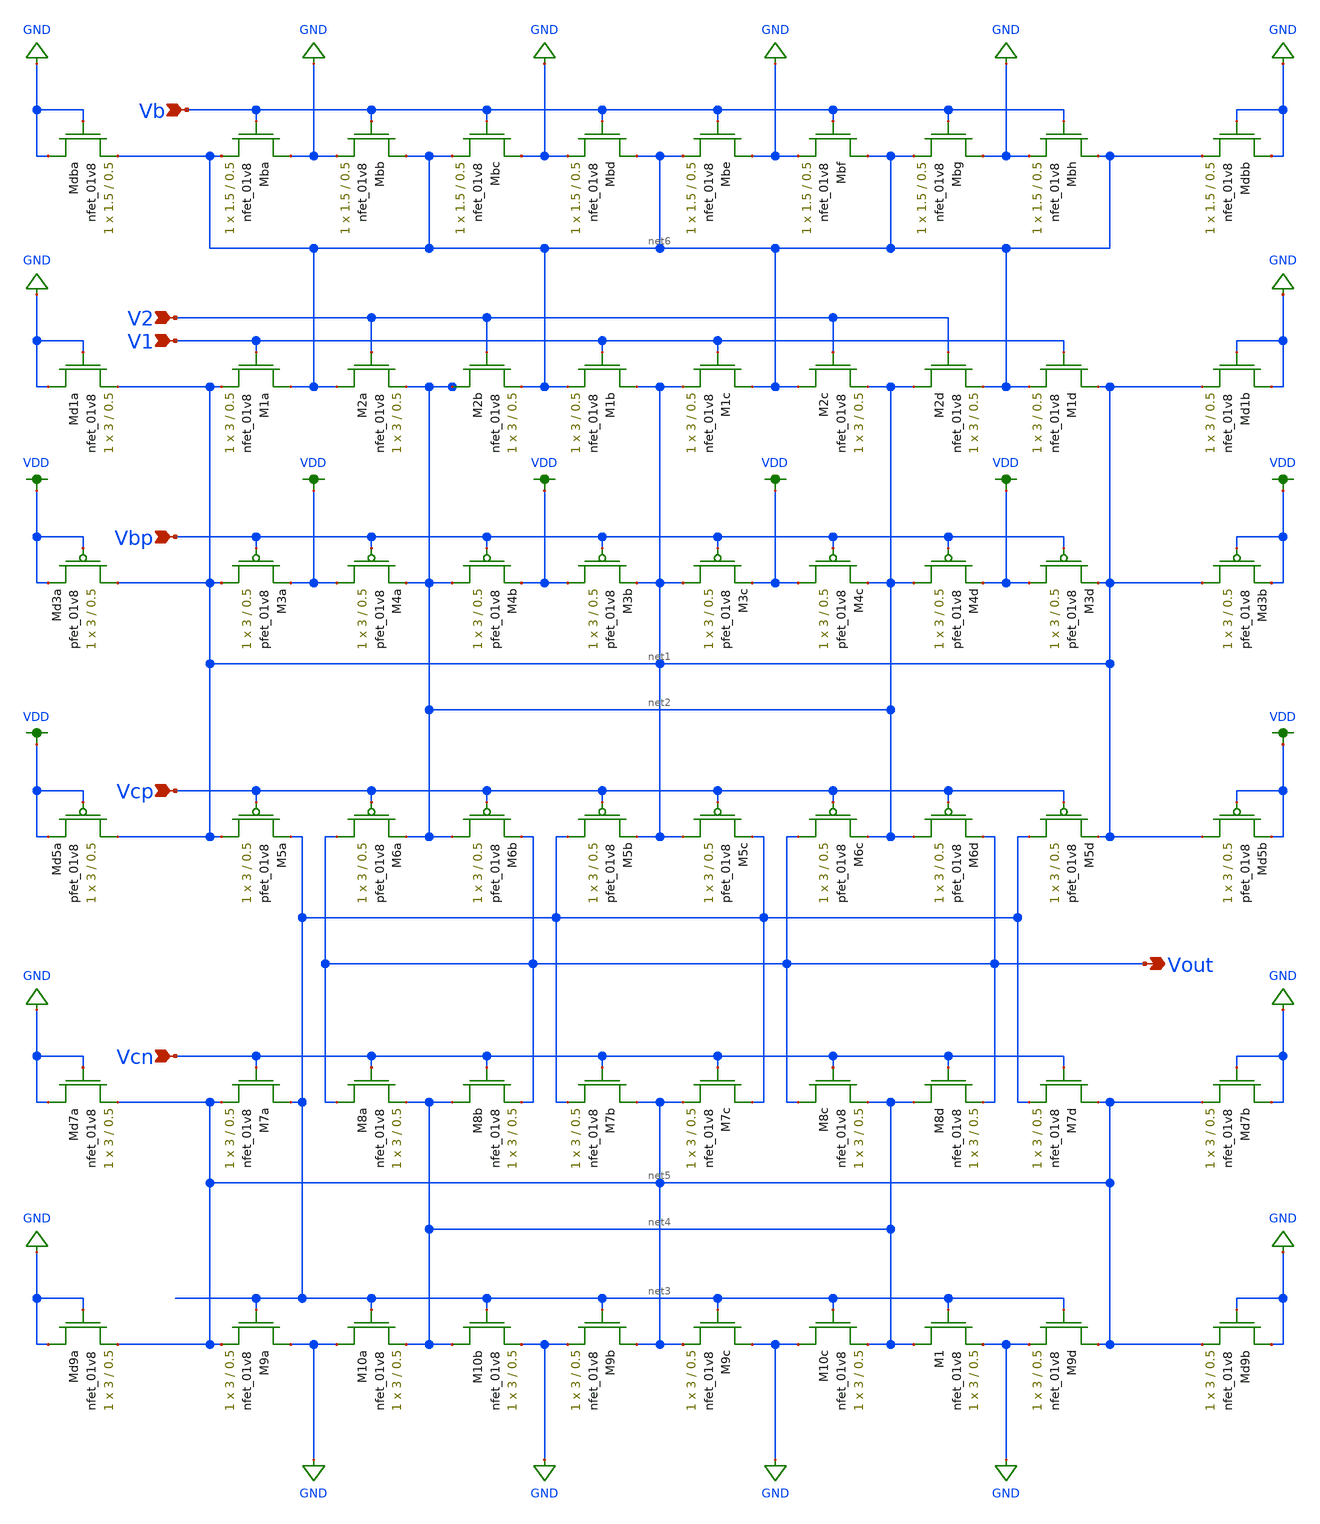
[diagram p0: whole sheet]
** sch_path: mp3/xschem/opamp_layout.sch
**.subckt opamp_layout Vbp Vcp Vcn V2 V1 Vb Vout
*.ipin Vbp
*.ipin Vcp
*.ipin Vcn
*.ipin V2
*.ipin V1
*.ipin Vb
*.opin Vout
XM1a net6 V1 net1 GND sky130_fd_pr__nfet_01v8 L=0.5 W=3 nf=1 ad='int((nf+1)/2) * W/nf * 0.29' as='int((nf+2)/2) * W/nf * 0.29'
+ pd='2*int((nf+1)/2) * (W/nf + 0.29)' ps='2*int((nf+2)/2) * (W/nf + 0.29)' nrd='0.29 / W' nrs='0.29 / W'
+ sa=0 sb=0 sd=0 mult=1 m=1
XM1b net1 V1 net6 GND sky130_fd_pr__nfet_01v8 L=0.5 W=3 nf=1 ad='int((nf+1)/2) * W/nf * 0.29' as='int((nf+2)/2) * W/nf * 0.29'
+ pd='2*int((nf+1)/2) * (W/nf + 0.29)' ps='2*int((nf+2)/2) * (W/nf + 0.29)' nrd='0.29 / W' nrs='0.29 / W'
+ sa=0 sb=0 sd=0 mult=1 m=1
XM1c net6 V1 net1 GND sky130_fd_pr__nfet_01v8 L=0.5 W=3 nf=1 ad='int((nf+1)/2) * W/nf * 0.29' as='int((nf+2)/2) * W/nf * 0.29'
+ pd='2*int((nf+1)/2) * (W/nf + 0.29)' ps='2*int((nf+2)/2) * (W/nf + 0.29)' nrd='0.29 / W' nrs='0.29 / W'
+ sa=0 sb=0 sd=0 mult=1 m=1
XM1d net1 V1 net6 GND sky130_fd_pr__nfet_01v8 L=0.5 W=3 nf=1 ad='int((nf+1)/2) * W/nf * 0.29' as='int((nf+2)/2) * W/nf * 0.29'
+ pd='2*int((nf+1)/2) * (W/nf + 0.29)' ps='2*int((nf+2)/2) * (W/nf + 0.29)' nrd='0.29 / W' nrs='0.29 / W'
+ sa=0 sb=0 sd=0 mult=1 m=1
XM2a net6 V2 net2 GND sky130_fd_pr__nfet_01v8 L=0.5 W=3 nf=1 ad='int((nf+1)/2) * W/nf * 0.29' as='int((nf+2)/2) * W/nf * 0.29'
+ pd='2*int((nf+1)/2) * (W/nf + 0.29)' ps='2*int((nf+2)/2) * (W/nf + 0.29)' nrd='0.29 / W' nrs='0.29 / W'
+ sa=0 sb=0 sd=0 mult=1 m=1
XM2b net2 V2 net6 GND sky130_fd_pr__nfet_01v8 L=0.5 W=3 nf=1 ad='int((nf+1)/2) * W/nf * 0.29' as='int((nf+2)/2) * W/nf * 0.29'
+ pd='2*int((nf+1)/2) * (W/nf + 0.29)' ps='2*int((nf+2)/2) * (W/nf + 0.29)' nrd='0.29 / W' nrs='0.29 / W'
+ sa=0 sb=0 sd=0 mult=1 m=1
XM2c net6 V2 net2 GND sky130_fd_pr__nfet_01v8 L=0.5 W=3 nf=1 ad='int((nf+1)/2) * W/nf * 0.29' as='int((nf+2)/2) * W/nf * 0.29'
+ pd='2*int((nf+1)/2) * (W/nf + 0.29)' ps='2*int((nf+2)/2) * (W/nf + 0.29)' nrd='0.29 / W' nrs='0.29 / W'
+ sa=0 sb=0 sd=0 mult=1 m=1
XM2d net2 V2 net6 GND sky130_fd_pr__nfet_01v8 L=0.5 W=3 nf=1 ad='int((nf+1)/2) * W/nf * 0.29' as='int((nf+2)/2) * W/nf * 0.29'
+ pd='2*int((nf+1)/2) * (W/nf + 0.29)' ps='2*int((nf+2)/2) * (W/nf + 0.29)' nrd='0.29 / W' nrs='0.29 / W'
+ sa=0 sb=0 sd=0 mult=1 m=1
XMba GND Vb net6 GND sky130_fd_pr__nfet_01v8 L=0.5 W=1.5 nf=1 ad='int((nf+1)/2) * W/nf * 0.29' as='int((nf+2)/2) * W/nf * 0.29'
+ pd='2*int((nf+1)/2) * (W/nf + 0.29)' ps='2*int((nf+2)/2) * (W/nf + 0.29)' nrd='0.29 / W' nrs='0.29 / W'
+ sa=0 sb=0 sd=0 mult=1 m=1
XMbb net6 Vb GND GND sky130_fd_pr__nfet_01v8 L=0.5 W=1.5 nf=1 ad='int((nf+1)/2) * W/nf * 0.29' as='int((nf+2)/2) * W/nf * 0.29'
+ pd='2*int((nf+1)/2) * (W/nf + 0.29)' ps='2*int((nf+2)/2) * (W/nf + 0.29)' nrd='0.29 / W' nrs='0.29 / W'
+ sa=0 sb=0 sd=0 mult=1 m=1
XMbc GND Vb net6 GND sky130_fd_pr__nfet_01v8 L=0.5 W=1.5 nf=1 ad='int((nf+1)/2) * W/nf * 0.29' as='int((nf+2)/2) * W/nf * 0.29'
+ pd='2*int((nf+1)/2) * (W/nf + 0.29)' ps='2*int((nf+2)/2) * (W/nf + 0.29)' nrd='0.29 / W' nrs='0.29 / W'
+ sa=0 sb=0 sd=0 mult=1 m=1
XMbd net6 Vb GND GND sky130_fd_pr__nfet_01v8 L=0.5 W=1.5 nf=1 ad='int((nf+1)/2) * W/nf * 0.29' as='int((nf+2)/2) * W/nf * 0.29'
+ pd='2*int((nf+1)/2) * (W/nf + 0.29)' ps='2*int((nf+2)/2) * (W/nf + 0.29)' nrd='0.29 / W' nrs='0.29 / W'
+ sa=0 sb=0 sd=0 mult=1 m=1
XMbe GND Vb net6 GND sky130_fd_pr__nfet_01v8 L=0.5 W=1.5 nf=1 ad='int((nf+1)/2) * W/nf * 0.29' as='int((nf+2)/2) * W/nf * 0.29'
+ pd='2*int((nf+1)/2) * (W/nf + 0.29)' ps='2*int((nf+2)/2) * (W/nf + 0.29)' nrd='0.29 / W' nrs='0.29 / W'
+ sa=0 sb=0 sd=0 mult=1 m=1
XMbf net6 Vb GND GND sky130_fd_pr__nfet_01v8 L=0.5 W=1.5 nf=1 ad='int((nf+1)/2) * W/nf * 0.29' as='int((nf+2)/2) * W/nf * 0.29'
+ pd='2*int((nf+1)/2) * (W/nf + 0.29)' ps='2*int((nf+2)/2) * (W/nf + 0.29)' nrd='0.29 / W' nrs='0.29 / W'
+ sa=0 sb=0 sd=0 mult=1 m=1
XMbg GND Vb net6 GND sky130_fd_pr__nfet_01v8 L=0.5 W=1.5 nf=1 ad='int((nf+1)/2) * W/nf * 0.29' as='int((nf+2)/2) * W/nf * 0.29'
+ pd='2*int((nf+1)/2) * (W/nf + 0.29)' ps='2*int((nf+2)/2) * (W/nf + 0.29)' nrd='0.29 / W' nrs='0.29 / W'
+ sa=0 sb=0 sd=0 mult=1 m=1
XMbh net6 Vb GND GND sky130_fd_pr__nfet_01v8 L=0.5 W=1.5 nf=1 ad='int((nf+1)/2) * W/nf * 0.29' as='int((nf+2)/2) * W/nf * 0.29'
+ pd='2*int((nf+1)/2) * (W/nf + 0.29)' ps='2*int((nf+2)/2) * (W/nf + 0.29)' nrd='0.29 / W' nrs='0.29 / W'
+ sa=0 sb=0 sd=0 mult=1 m=1
XM7a net3 Vcn net5 GND sky130_fd_pr__nfet_01v8 L=0.5 W=3 nf=1 ad='int((nf+1)/2) * W/nf * 0.29' as='int((nf+2)/2) * W/nf * 0.29'
+ pd='2*int((nf+1)/2) * (W/nf + 0.29)' ps='2*int((nf+2)/2) * (W/nf + 0.29)' nrd='0.29 / W' nrs='0.29 / W'
+ sa=0 sb=0 sd=0 mult=1 m=1
XM7b net5 Vcn net3 GND sky130_fd_pr__nfet_01v8 L=0.5 W=3 nf=1 ad='int((nf+1)/2) * W/nf * 0.29' as='int((nf+2)/2) * W/nf * 0.29'
+ pd='2*int((nf+1)/2) * (W/nf + 0.29)' ps='2*int((nf+2)/2) * (W/nf + 0.29)' nrd='0.29 / W' nrs='0.29 / W'
+ sa=0 sb=0 sd=0 mult=1 m=1
XM7c net3 Vcn net5 GND sky130_fd_pr__nfet_01v8 L=0.5 W=3 nf=1 ad='int((nf+1)/2) * W/nf * 0.29' as='int((nf+2)/2) * W/nf * 0.29'
+ pd='2*int((nf+1)/2) * (W/nf + 0.29)' ps='2*int((nf+2)/2) * (W/nf + 0.29)' nrd='0.29 / W' nrs='0.29 / W'
+ sa=0 sb=0 sd=0 mult=1 m=1
XM7d net5 Vcn net3 GND sky130_fd_pr__nfet_01v8 L=0.5 W=3 nf=1 ad='int((nf+1)/2) * W/nf * 0.29' as='int((nf+2)/2) * W/nf * 0.29'
+ pd='2*int((nf+1)/2) * (W/nf + 0.29)' ps='2*int((nf+2)/2) * (W/nf + 0.29)' nrd='0.29 / W' nrs='0.29 / W'
+ sa=0 sb=0 sd=0 mult=1 m=1
XM8a Vout Vcn net4 GND sky130_fd_pr__nfet_01v8 L=0.5 W=3 nf=1 ad='int((nf+1)/2) * W/nf * 0.29' as='int((nf+2)/2) * W/nf * 0.29'
+ pd='2*int((nf+1)/2) * (W/nf + 0.29)' ps='2*int((nf+2)/2) * (W/nf + 0.29)' nrd='0.29 / W' nrs='0.29 / W'
+ sa=0 sb=0 sd=0 mult=1 m=1
XM8b net4 Vcn Vout GND sky130_fd_pr__nfet_01v8 L=0.5 W=3 nf=1 ad='int((nf+1)/2) * W/nf * 0.29' as='int((nf+2)/2) * W/nf * 0.29'
+ pd='2*int((nf+1)/2) * (W/nf + 0.29)' ps='2*int((nf+2)/2) * (W/nf + 0.29)' nrd='0.29 / W' nrs='0.29 / W'
+ sa=0 sb=0 sd=0 mult=1 m=1
XM8c Vout Vcn net4 GND sky130_fd_pr__nfet_01v8 L=0.5 W=3 nf=1 ad='int((nf+1)/2) * W/nf * 0.29' as='int((nf+2)/2) * W/nf * 0.29'
+ pd='2*int((nf+1)/2) * (W/nf + 0.29)' ps='2*int((nf+2)/2) * (W/nf + 0.29)' nrd='0.29 / W' nrs='0.29 / W'
+ sa=0 sb=0 sd=0 mult=1 m=1
XM8d net4 Vcn Vout GND sky130_fd_pr__nfet_01v8 L=0.5 W=3 nf=1 ad='int((nf+1)/2) * W/nf * 0.29' as='int((nf+2)/2) * W/nf * 0.29'
+ pd='2*int((nf+1)/2) * (W/nf + 0.29)' ps='2*int((nf+2)/2) * (W/nf + 0.29)' nrd='0.29 / W' nrs='0.29 / W'
+ sa=0 sb=0 sd=0 mult=1 m=1
XM9a GND net3 net5 GND sky130_fd_pr__nfet_01v8 L=0.5 W=3 nf=1 ad='int((nf+1)/2) * W/nf * 0.29' as='int((nf+2)/2) * W/nf * 0.29'
+ pd='2*int((nf+1)/2) * (W/nf + 0.29)' ps='2*int((nf+2)/2) * (W/nf + 0.29)' nrd='0.29 / W' nrs='0.29 / W'
+ sa=0 sb=0 sd=0 mult=1 m=1
XM9b net5 net3 GND GND sky130_fd_pr__nfet_01v8 L=0.5 W=3 nf=1 ad='int((nf+1)/2) * W/nf * 0.29' as='int((nf+2)/2) * W/nf * 0.29'
+ pd='2*int((nf+1)/2) * (W/nf + 0.29)' ps='2*int((nf+2)/2) * (W/nf + 0.29)' nrd='0.29 / W' nrs='0.29 / W'
+ sa=0 sb=0 sd=0 mult=1 m=1
XM9c GND net3 net5 GND sky130_fd_pr__nfet_01v8 L=0.5 W=3 nf=1 ad='int((nf+1)/2) * W/nf * 0.29' as='int((nf+2)/2) * W/nf * 0.29'
+ pd='2*int((nf+1)/2) * (W/nf + 0.29)' ps='2*int((nf+2)/2) * (W/nf + 0.29)' nrd='0.29 / W' nrs='0.29 / W'
+ sa=0 sb=0 sd=0 mult=1 m=1
XM9d net5 net3 GND GND sky130_fd_pr__nfet_01v8 L=0.5 W=3 nf=1 ad='int((nf+1)/2) * W/nf * 0.29' as='int((nf+2)/2) * W/nf * 0.29'
+ pd='2*int((nf+1)/2) * (W/nf + 0.29)' ps='2*int((nf+2)/2) * (W/nf + 0.29)' nrd='0.29 / W' nrs='0.29 / W'
+ sa=0 sb=0 sd=0 mult=1 m=1
XM10a GND net3 net4 GND sky130_fd_pr__nfet_01v8 L=0.5 W=3 nf=1 ad='int((nf+1)/2) * W/nf * 0.29' as='int((nf+2)/2) * W/nf * 0.29'
+ pd='2*int((nf+1)/2) * (W/nf + 0.29)' ps='2*int((nf+2)/2) * (W/nf + 0.29)' nrd='0.29 / W' nrs='0.29 / W'
+ sa=0 sb=0 sd=0 mult=1 m=1
XM10b net4 net3 GND GND sky130_fd_pr__nfet_01v8 L=0.5 W=3 nf=1 ad='int((nf+1)/2) * W/nf * 0.29' as='int((nf+2)/2) * W/nf * 0.29'
+ pd='2*int((nf+1)/2) * (W/nf + 0.29)' ps='2*int((nf+2)/2) * (W/nf + 0.29)' nrd='0.29 / W' nrs='0.29 / W'
+ sa=0 sb=0 sd=0 mult=1 m=1
XM10c GND net3 net4 GND sky130_fd_pr__nfet_01v8 L=0.5 W=3 nf=1 ad='int((nf+1)/2) * W/nf * 0.29' as='int((nf+2)/2) * W/nf * 0.29'
+ pd='2*int((nf+1)/2) * (W/nf + 0.29)' ps='2*int((nf+2)/2) * (W/nf + 0.29)' nrd='0.29 / W' nrs='0.29 / W'
+ sa=0 sb=0 sd=0 mult=1 m=1
XM1 net4 net3 GND GND sky130_fd_pr__nfet_01v8 L=0.5 W=3 nf=1 ad='int((nf+1)/2) * W/nf * 0.29' as='int((nf+2)/2) * W/nf * 0.29'
+ pd='2*int((nf+1)/2) * (W/nf + 0.29)' ps='2*int((nf+2)/2) * (W/nf + 0.29)' nrd='0.29 / W' nrs='0.29 / W'
+ sa=0 sb=0 sd=0 mult=1 m=1
XM5a net1 Vcp net3 VDD sky130_fd_pr__pfet_01v8 L=0.5 W=3 nf=1 ad='int((nf+1)/2) * W/nf * 0.29' as='int((nf+2)/2) * W/nf * 0.29'
+ pd='2*int((nf+1)/2) * (W/nf + 0.29)' ps='2*int((nf+2)/2) * (W/nf + 0.29)' nrd='0.29 / W' nrs='0.29 / W'
+ sa=0 sb=0 sd=0 mult=1 m=1
XM5b net3 Vcp net1 VDD sky130_fd_pr__pfet_01v8 L=0.5 W=3 nf=1 ad='int((nf+1)/2) * W/nf * 0.29' as='int((nf+2)/2) * W/nf * 0.29'
+ pd='2*int((nf+1)/2) * (W/nf + 0.29)' ps='2*int((nf+2)/2) * (W/nf + 0.29)' nrd='0.29 / W' nrs='0.29 / W'
+ sa=0 sb=0 sd=0 mult=1 m=1
XM5c net1 Vcp net3 VDD sky130_fd_pr__pfet_01v8 L=0.5 W=3 nf=1 ad='int((nf+1)/2) * W/nf * 0.29' as='int((nf+2)/2) * W/nf * 0.29'
+ pd='2*int((nf+1)/2) * (W/nf + 0.29)' ps='2*int((nf+2)/2) * (W/nf + 0.29)' nrd='0.29 / W' nrs='0.29 / W'
+ sa=0 sb=0 sd=0 mult=1 m=1
XM5d net3 Vcp net1 VDD sky130_fd_pr__pfet_01v8 L=0.5 W=3 nf=1 ad='int((nf+1)/2) * W/nf * 0.29' as='int((nf+2)/2) * W/nf * 0.29'
+ pd='2*int((nf+1)/2) * (W/nf + 0.29)' ps='2*int((nf+2)/2) * (W/nf + 0.29)' nrd='0.29 / W' nrs='0.29 / W'
+ sa=0 sb=0 sd=0 mult=1 m=1
XM6a Vout Vcp net2 VDD sky130_fd_pr__pfet_01v8 L=0.5 W=3 nf=1 ad='int((nf+1)/2) * W/nf * 0.29' as='int((nf+2)/2) * W/nf * 0.29'
+ pd='2*int((nf+1)/2) * (W/nf + 0.29)' ps='2*int((nf+2)/2) * (W/nf + 0.29)' nrd='0.29 / W' nrs='0.29 / W'
+ sa=0 sb=0 sd=0 mult=1 m=1
XM6b net2 Vcp Vout VDD sky130_fd_pr__pfet_01v8 L=0.5 W=3 nf=1 ad='int((nf+1)/2) * W/nf * 0.29' as='int((nf+2)/2) * W/nf * 0.29'
+ pd='2*int((nf+1)/2) * (W/nf + 0.29)' ps='2*int((nf+2)/2) * (W/nf + 0.29)' nrd='0.29 / W' nrs='0.29 / W'
+ sa=0 sb=0 sd=0 mult=1 m=1
XM6c Vout Vcp net2 VDD sky130_fd_pr__pfet_01v8 L=0.5 W=3 nf=1 ad='int((nf+1)/2) * W/nf * 0.29' as='int((nf+2)/2) * W/nf * 0.29'
+ pd='2*int((nf+1)/2) * (W/nf + 0.29)' ps='2*int((nf+2)/2) * (W/nf + 0.29)' nrd='0.29 / W' nrs='0.29 / W'
+ sa=0 sb=0 sd=0 mult=1 m=1
XM6d net2 Vcp Vout VDD sky130_fd_pr__pfet_01v8 L=0.5 W=3 nf=1 ad='int((nf+1)/2) * W/nf * 0.29' as='int((nf+2)/2) * W/nf * 0.29'
+ pd='2*int((nf+1)/2) * (W/nf + 0.29)' ps='2*int((nf+2)/2) * (W/nf + 0.29)' nrd='0.29 / W' nrs='0.29 / W'
+ sa=0 sb=0 sd=0 mult=1 m=1
XM3a net1 Vbp VDD VDD sky130_fd_pr__pfet_01v8 L=0.5 W=3 nf=1 ad='int((nf+1)/2) * W/nf * 0.29' as='int((nf+2)/2) * W/nf * 0.29'
+ pd='2*int((nf+1)/2) * (W/nf + 0.29)' ps='2*int((nf+2)/2) * (W/nf + 0.29)' nrd='0.29 / W' nrs='0.29 / W'
+ sa=0 sb=0 sd=0 mult=1 m=1
XM3b VDD Vbp net1 VDD sky130_fd_pr__pfet_01v8 L=0.5 W=3 nf=1 ad='int((nf+1)/2) * W/nf * 0.29' as='int((nf+2)/2) * W/nf * 0.29'
+ pd='2*int((nf+1)/2) * (W/nf + 0.29)' ps='2*int((nf+2)/2) * (W/nf + 0.29)' nrd='0.29 / W' nrs='0.29 / W'
+ sa=0 sb=0 sd=0 mult=1 m=1
XM3c net1 Vbp VDD VDD sky130_fd_pr__pfet_01v8 L=0.5 W=3 nf=1 ad='int((nf+1)/2) * W/nf * 0.29' as='int((nf+2)/2) * W/nf * 0.29'
+ pd='2*int((nf+1)/2) * (W/nf + 0.29)' ps='2*int((nf+2)/2) * (W/nf + 0.29)' nrd='0.29 / W' nrs='0.29 / W'
+ sa=0 sb=0 sd=0 mult=1 m=1
XM3d VDD Vbp net1 VDD sky130_fd_pr__pfet_01v8 L=0.5 W=3 nf=1 ad='int((nf+1)/2) * W/nf * 0.29' as='int((nf+2)/2) * W/nf * 0.29'
+ pd='2*int((nf+1)/2) * (W/nf + 0.29)' ps='2*int((nf+2)/2) * (W/nf + 0.29)' nrd='0.29 / W' nrs='0.29 / W'
+ sa=0 sb=0 sd=0 mult=1 m=1
XM4a VDD Vbp net2 VDD sky130_fd_pr__pfet_01v8 L=0.5 W=3 nf=1 ad='int((nf+1)/2) * W/nf * 0.29' as='int((nf+2)/2) * W/nf * 0.29'
+ pd='2*int((nf+1)/2) * (W/nf + 0.29)' ps='2*int((nf+2)/2) * (W/nf + 0.29)' nrd='0.29 / W' nrs='0.29 / W'
+ sa=0 sb=0 sd=0 mult=1 m=1
XM4b net2 Vbp VDD VDD sky130_fd_pr__pfet_01v8 L=0.5 W=3 nf=1 ad='int((nf+1)/2) * W/nf * 0.29' as='int((nf+2)/2) * W/nf * 0.29'
+ pd='2*int((nf+1)/2) * (W/nf + 0.29)' ps='2*int((nf+2)/2) * (W/nf + 0.29)' nrd='0.29 / W' nrs='0.29 / W'
+ sa=0 sb=0 sd=0 mult=1 m=1
XM4c VDD Vbp net2 VDD sky130_fd_pr__pfet_01v8 L=0.5 W=3 nf=1 ad='int((nf+1)/2) * W/nf * 0.29' as='int((nf+2)/2) * W/nf * 0.29'
+ pd='2*int((nf+1)/2) * (W/nf + 0.29)' ps='2*int((nf+2)/2) * (W/nf + 0.29)' nrd='0.29 / W' nrs='0.29 / W'
+ sa=0 sb=0 sd=0 mult=1 m=1
XM4d net2 Vbp VDD VDD sky130_fd_pr__pfet_01v8 L=0.5 W=3 nf=1 ad='int((nf+1)/2) * W/nf * 0.29' as='int((nf+2)/2) * W/nf * 0.29'
+ pd='2*int((nf+1)/2) * (W/nf + 0.29)' ps='2*int((nf+2)/2) * (W/nf + 0.29)' nrd='0.29 / W' nrs='0.29 / W'
+ sa=0 sb=0 sd=0 mult=1 m=1
XMdbb GND GND net6 GND sky130_fd_pr__nfet_01v8 L=0.5 W=1.5 nf=1 ad='int((nf+1)/2) * W/nf * 0.29' as='int((nf+2)/2) * W/nf * 0.29'
+ pd='2*int((nf+1)/2) * (W/nf + 0.29)' ps='2*int((nf+2)/2) * (W/nf + 0.29)' nrd='0.29 / W' nrs='0.29 / W'
+ sa=0 sb=0 sd=0 mult=1 m=1
XMd1b GND GND net1 GND sky130_fd_pr__nfet_01v8 L=0.5 W=3 nf=1 ad='int((nf+1)/2) * W/nf * 0.29' as='int((nf+2)/2) * W/nf * 0.29'
+ pd='2*int((nf+1)/2) * (W/nf + 0.29)' ps='2*int((nf+2)/2) * (W/nf + 0.29)' nrd='0.29 / W' nrs='0.29 / W'
+ sa=0 sb=0 sd=0 mult=1 m=1
XMd7b GND GND net5 GND sky130_fd_pr__nfet_01v8 L=0.5 W=3 nf=1 ad='int((nf+1)/2) * W/nf * 0.29' as='int((nf+2)/2) * W/nf * 0.29'
+ pd='2*int((nf+1)/2) * (W/nf + 0.29)' ps='2*int((nf+2)/2) * (W/nf + 0.29)' nrd='0.29 / W' nrs='0.29 / W'
+ sa=0 sb=0 sd=0 mult=1 m=1
XMd9b GND GND net5 GND sky130_fd_pr__nfet_01v8 L=0.5 W=3 nf=1 ad='int((nf+1)/2) * W/nf * 0.29' as='int((nf+2)/2) * W/nf * 0.29'
+ pd='2*int((nf+1)/2) * (W/nf + 0.29)' ps='2*int((nf+2)/2) * (W/nf + 0.29)' nrd='0.29 / W' nrs='0.29 / W'
+ sa=0 sb=0 sd=0 mult=1 m=1
XMd3b net1 VDD VDD VDD sky130_fd_pr__pfet_01v8 L=0.5 W=3 nf=1 ad='int((nf+1)/2) * W/nf * 0.29' as='int((nf+2)/2) * W/nf * 0.29'
+ pd='2*int((nf+1)/2) * (W/nf + 0.29)' ps='2*int((nf+2)/2) * (W/nf + 0.29)' nrd='0.29 / W' nrs='0.29 / W'
+ sa=0 sb=0 sd=0 mult=1 m=1
XMd5b net1 VDD VDD VDD sky130_fd_pr__pfet_01v8 L=0.5 W=3 nf=1 ad='int((nf+1)/2) * W/nf * 0.29' as='int((nf+2)/2) * W/nf * 0.29'
+ pd='2*int((nf+1)/2) * (W/nf + 0.29)' ps='2*int((nf+2)/2) * (W/nf + 0.29)' nrd='0.29 / W' nrs='0.29 / W'
+ sa=0 sb=0 sd=0 mult=1 m=1
XMdba GND GND net6 GND sky130_fd_pr__nfet_01v8 L=0.5 W=1.5 nf=1 ad='int((nf+1)/2) * W/nf * 0.29' as='int((nf+2)/2) * W/nf * 0.29'
+ pd='2*int((nf+1)/2) * (W/nf + 0.29)' ps='2*int((nf+2)/2) * (W/nf + 0.29)' nrd='0.29 / W' nrs='0.29 / W'
+ sa=0 sb=0 sd=0 mult=1 m=1
XMd1a GND GND net1 GND sky130_fd_pr__nfet_01v8 L=0.5 W=3 nf=1 ad='int((nf+1)/2) * W/nf * 0.29' as='int((nf+2)/2) * W/nf * 0.29'
+ pd='2*int((nf+1)/2) * (W/nf + 0.29)' ps='2*int((nf+2)/2) * (W/nf + 0.29)' nrd='0.29 / W' nrs='0.29 / W'
+ sa=0 sb=0 sd=0 mult=1 m=1
XMd7a GND GND net5 GND sky130_fd_pr__nfet_01v8 L=0.5 W=3 nf=1 ad='int((nf+1)/2) * W/nf * 0.29' as='int((nf+2)/2) * W/nf * 0.29'
+ pd='2*int((nf+1)/2) * (W/nf + 0.29)' ps='2*int((nf+2)/2) * (W/nf + 0.29)' nrd='0.29 / W' nrs='0.29 / W'
+ sa=0 sb=0 sd=0 mult=1 m=1
XMd9a GND GND net5 GND sky130_fd_pr__nfet_01v8 L=0.5 W=3 nf=1 ad='int((nf+1)/2) * W/nf * 0.29' as='int((nf+2)/2) * W/nf * 0.29'
+ pd='2*int((nf+1)/2) * (W/nf + 0.29)' ps='2*int((nf+2)/2) * (W/nf + 0.29)' nrd='0.29 / W' nrs='0.29 / W'
+ sa=0 sb=0 sd=0 mult=1 m=1
XMd3a net1 VDD VDD VDD sky130_fd_pr__pfet_01v8 L=0.5 W=3 nf=1 ad='int((nf+1)/2) * W/nf * 0.29' as='int((nf+2)/2) * W/nf * 0.29'
+ pd='2*int((nf+1)/2) * (W/nf + 0.29)' ps='2*int((nf+2)/2) * (W/nf + 0.29)' nrd='0.29 / W' nrs='0.29 / W'
+ sa=0 sb=0 sd=0 mult=1 m=1
XMd5a net1 VDD VDD VDD sky130_fd_pr__pfet_01v8 L=0.5 W=3 nf=1 ad='int((nf+1)/2) * W/nf * 0.29' as='int((nf+2)/2) * W/nf * 0.29'
+ pd='2*int((nf+1)/2) * (W/nf + 0.29)' ps='2*int((nf+2)/2) * (W/nf + 0.29)' nrd='0.29 / W' nrs='0.29 / W'
+ sa=0 sb=0 sd=0 mult=1 m=1
**.ends
.GLOBAL VDD
.GLOBAL GND
.end
